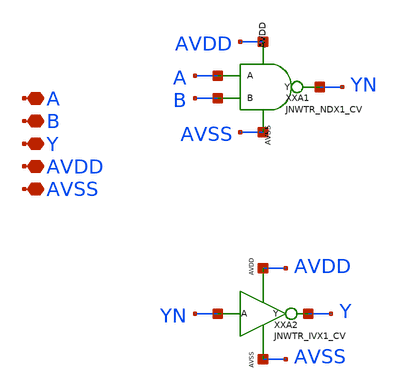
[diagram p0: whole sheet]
** sch_path: design/JNW_TR_SKY130A/JNWTR_ANX8_CV.sch
**.subckt JNWTR_ANX8_CV A B Y AVDD AVSS
*.iopin A
*.iopin B
*.iopin Y
*.iopin AVDD
*.iopin AVSS
XXA1 A B YN AVDD AVSS JNWTR_NDX1_CV
XXA2 YN Y AVDD AVSS JNWTR_IVX1_CV
**.ends
.end
